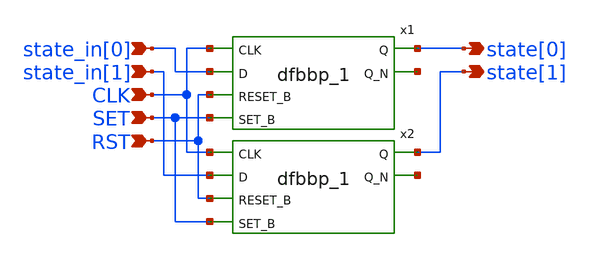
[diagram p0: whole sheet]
** sch_path: XSCHEM/state_reg.sch
**.subckt state_reg state_in[0] state_in[1] CLK SET RST state[0] state[1]
*.ipin state_in[0]
*.ipin state_in[1]
*.ipin CLK
*.ipin SET
*.ipin RST
*.opin state[0]
*.opin state[1]
x1 CLK state_in[0] RST SET VGND VNB VPB VPWR state[0] net1 sky130_fd_sc_hd__dfbbp_1
x2 CLK state_in[1] RST SET VGND VNB VPB VPWR state[1] net2 sky130_fd_sc_hd__dfbbp_1
**.ends
.end
